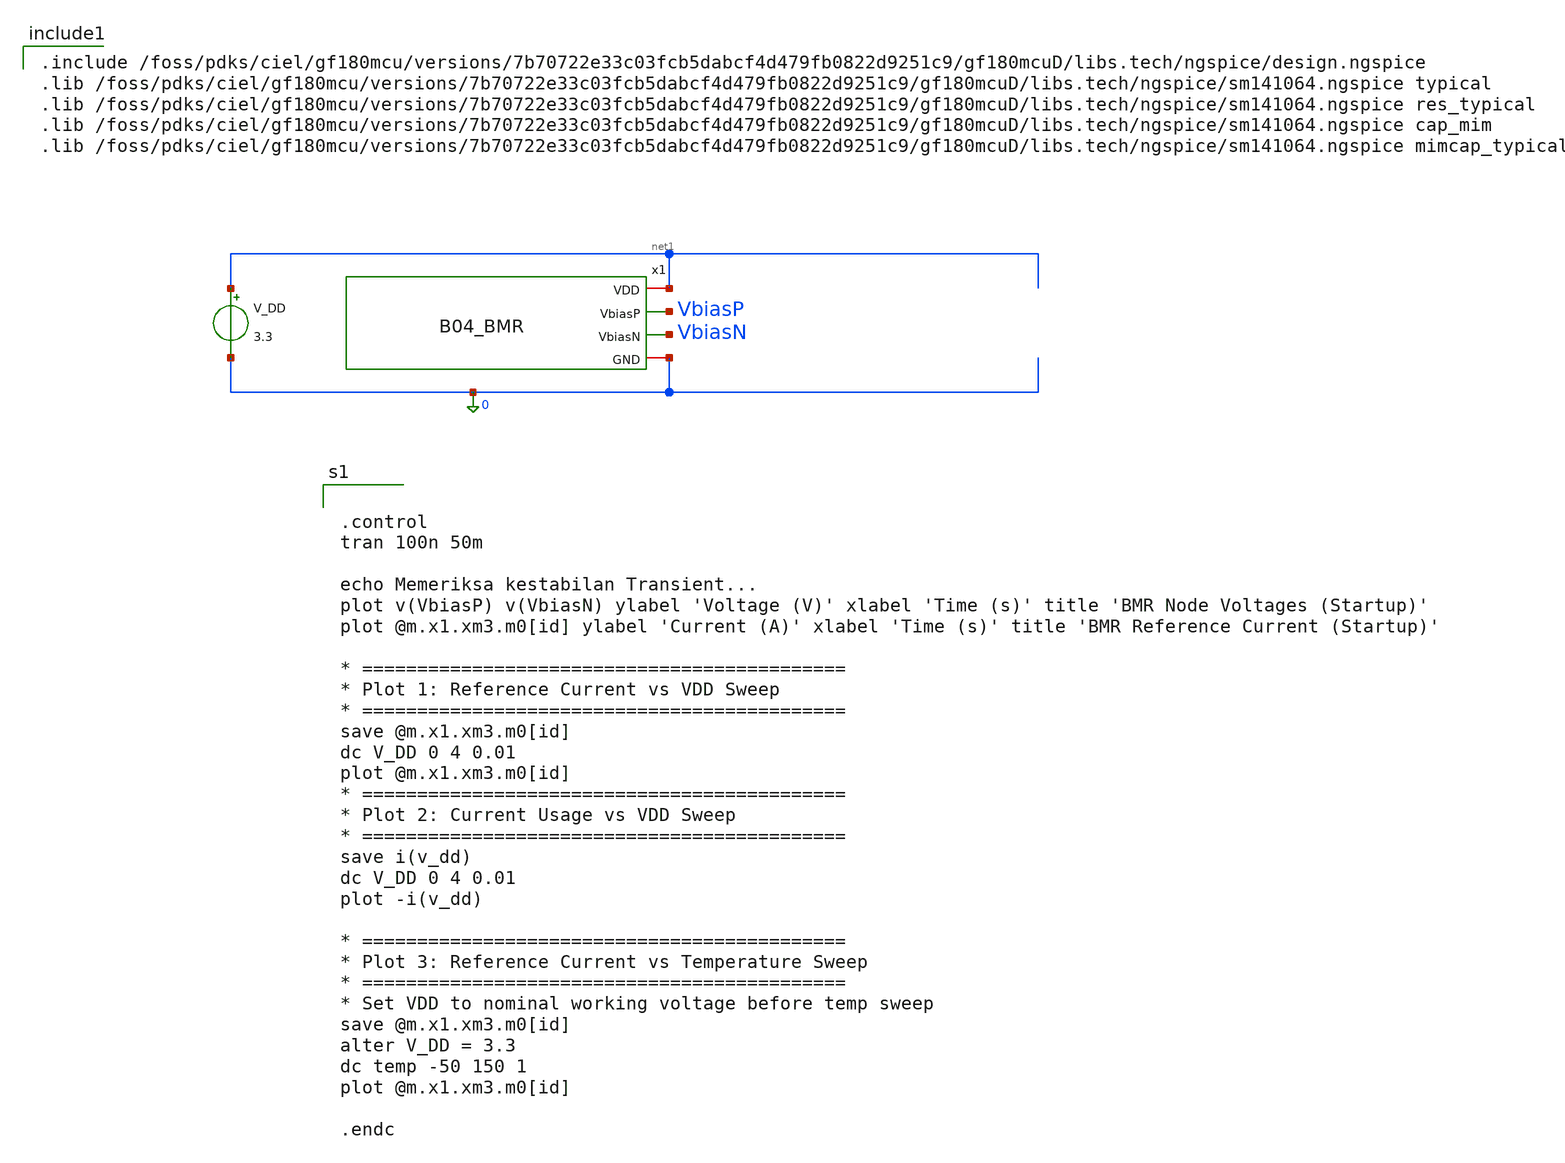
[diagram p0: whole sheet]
** sch_path: analog/B04_tb_beta_multiplier_reference.sch
**.subckt B04_tb_beta_multiplier_reference
V_DD net1 0 3.3
x1 net1 VbiasP VbiasN 0 B04_BMR
**** begin user architecture code


.control
tran 100n 50m

echo Memeriksa kestabilan Transient...
plot v(VbiasP) v(VbiasN) ylabel 'Voltage (V)' xlabel 'Time (s)' title 'BMR Node Voltages (Startup)'
plot @m.x1.xm3.m0[id] ylabel 'Current (A)' xlabel 'Time (s)' title 'BMR Reference Current (Startup)'

* ============================================
* Plot 1: Reference Current vs VDD Sweep
* ============================================
save @m.x1.xm3.m0[id]
dc V_DD 0 4 0.01
plot @m.x1.xm3.m0[id]
* ============================================
* Plot 2: Current Usage vs VDD Sweep
* ============================================
save i(v_dd)
dc V_DD 0 4 0.01
plot -i(v_dd)

* ============================================
* Plot 3: Reference Current vs Temperature Sweep
* ============================================
* Set VDD to nominal working voltage before temp sweep
save @m.x1.xm3.m0[id]
alter V_DD = 3.3
dc temp -50 150 1
plot @m.x1.xm3.m0[id]

.endc




.include /foss/pdks/ciel/gf180mcu/versions/7b70722e33c03fcb5dabcf4d479fb0822d9251c9/gf180mcuD/libs.tech/ngspice/design.ngspice
.lib /foss/pdks/ciel/gf180mcu/versions/7b70722e33c03fcb5dabcf4d479fb0822d9251c9/gf180mcuD/libs.tech/ngspice/sm141064.ngspice typical
.lib /foss/pdks/ciel/gf180mcu/versions/7b70722e33c03fcb5dabcf4d479fb0822d9251c9/gf180mcuD/libs.tech/ngspice/sm141064.ngspice res_typical
.lib /foss/pdks/ciel/gf180mcu/versions/7b70722e33c03fcb5dabcf4d479fb0822d9251c9/gf180mcuD/libs.tech/ngspice/sm141064.ngspice cap_mim
.lib /foss/pdks/ciel/gf180mcu/versions/7b70722e33c03fcb5dabcf4d479fb0822d9251c9/gf180mcuD/libs.tech/ngspice/sm141064.ngspice mimcap_typical

**** end user architecture code
**.ends
.end
